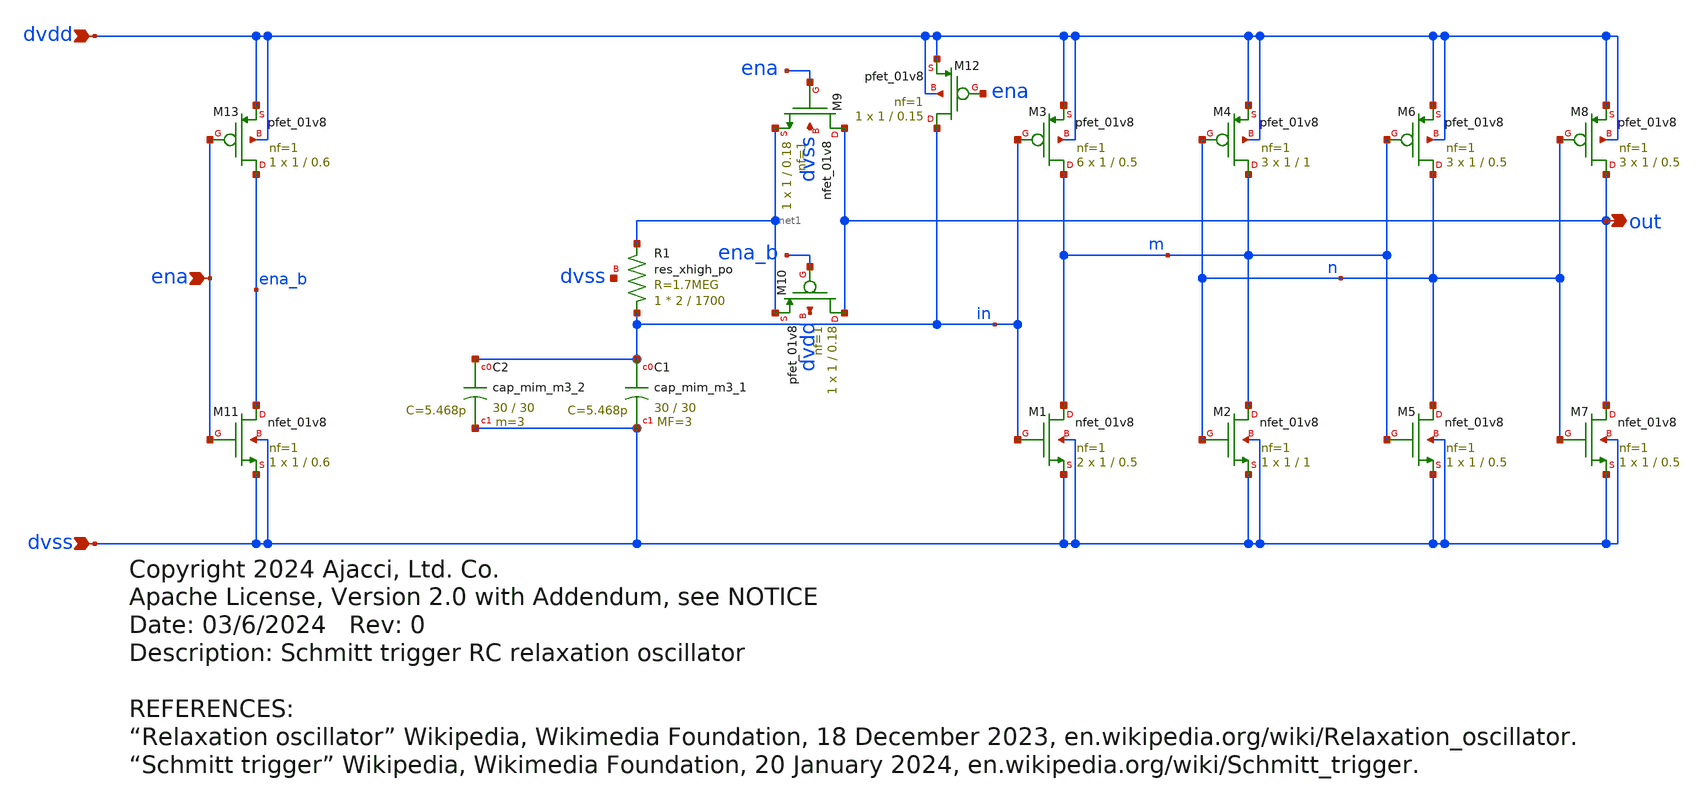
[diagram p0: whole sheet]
** sch_path: xschem/rc_osc.sch
* Copyright 2024 Ajacci, Ltd. Co.
* Apache License, Version 2.0 with Addendum, see NOTICE
**.subckt rc_osc dvdd dvss out ena
*.ipin dvdd
*.ipin dvss
*.opin out
*.ipin ena
XM1 m in dvss dvss sky130_fd_pr__nfet_01v8 L=0.5 W=1 nf=1 ad='int((nf+1)/2) * W/nf * 0.29' as='int((nf+2)/2) * W/nf * 0.29'
+ pd='2*int((nf+1)/2) * (W/nf + 0.29)' ps='2*int((nf+2)/2) * (W/nf + 0.29)' nrd='0.29 / W' nrs='0.29 / W'
+ sa=0 sb=0 sd=0 mult=2 m=2
XM3 m in dvdd dvdd sky130_fd_pr__pfet_01v8 L=0.5 W=1 nf=1 ad='int((nf+1)/2) * W/nf * 0.29' as='int((nf+2)/2) * W/nf * 0.29'
+ pd='2*int((nf+1)/2) * (W/nf + 0.29)' ps='2*int((nf+2)/2) * (W/nf + 0.29)' nrd='0.29 / W' nrs='0.29 / W'
+ sa=0 sb=0 sd=0 mult=6 m=6
XM2 m n dvss dvss sky130_fd_pr__nfet_01v8 L=1 W=1 nf=1 ad='int((nf+1)/2) * W/nf * 0.29' as='int((nf+2)/2) * W/nf * 0.29'
+ pd='2*int((nf+1)/2) * (W/nf + 0.29)' ps='2*int((nf+2)/2) * (W/nf + 0.29)' nrd='0.29 / W' nrs='0.29 / W'
+ sa=0 sb=0 sd=0 mult=1 m=1
XM4 m n dvdd dvdd sky130_fd_pr__pfet_01v8 L=1 W=1 nf=1 ad='int((nf+1)/2) * W/nf * 0.29' as='int((nf+2)/2) * W/nf * 0.29'
+ pd='2*int((nf+1)/2) * (W/nf + 0.29)' ps='2*int((nf+2)/2) * (W/nf + 0.29)' nrd='0.29 / W' nrs='0.29 / W'
+ sa=0 sb=0 sd=0 mult=3 m=3
XM5 n m dvss dvss sky130_fd_pr__nfet_01v8 L=0.5 W=1 nf=1 ad='int((nf+1)/2) * W/nf * 0.29' as='int((nf+2)/2) * W/nf * 0.29'
+ pd='2*int((nf+1)/2) * (W/nf + 0.29)' ps='2*int((nf+2)/2) * (W/nf + 0.29)' nrd='0.29 / W' nrs='0.29 / W'
+ sa=0 sb=0 sd=0 mult=1 m=1
XM6 n m dvdd dvdd sky130_fd_pr__pfet_01v8 L=0.5 W=1 nf=1 ad='int((nf+1)/2) * W/nf * 0.29' as='int((nf+2)/2) * W/nf * 0.29'
+ pd='2*int((nf+1)/2) * (W/nf + 0.29)' ps='2*int((nf+2)/2) * (W/nf + 0.29)' nrd='0.29 / W' nrs='0.29 / W'
+ sa=0 sb=0 sd=0 mult=3 m=3
XM7 out n dvss dvss sky130_fd_pr__nfet_01v8 L=0.5 W=1 nf=1 ad='int((nf+1)/2) * W/nf * 0.29' as='int((nf+2)/2) * W/nf * 0.29'
+ pd='2*int((nf+1)/2) * (W/nf + 0.29)' ps='2*int((nf+2)/2) * (W/nf + 0.29)' nrd='0.29 / W' nrs='0.29 / W'
+ sa=0 sb=0 sd=0 mult=1 m=1
XM8 out n dvdd dvdd sky130_fd_pr__pfet_01v8 L=0.5 W=1 nf=1 ad='int((nf+1)/2) * W/nf * 0.29' as='int((nf+2)/2) * W/nf * 0.29'
+ pd='2*int((nf+1)/2) * (W/nf + 0.29)' ps='2*int((nf+2)/2) * (W/nf + 0.29)' nrd='0.29 / W' nrs='0.29 / W'
+ sa=0 sb=0 sd=0 mult=3 m=3
XC1 in dvss sky130_fd_pr__cap_mim_m3_1 W=30 L=30 MF=3 m=3
XR1 in net1 dvss sky130_fd_pr__res_xhigh_po W=2 L=1700 mult=1 m=1
XM12 in ena dvdd dvdd sky130_fd_pr__pfet_01v8 L=0.15 W=1 nf=1 ad='int((nf+1)/2) * W/nf * 0.29' as='int((nf+2)/2) * W/nf * 0.29'
+ pd='2*int((nf+1)/2) * (W/nf + 0.29)' ps='2*int((nf+2)/2) * (W/nf + 0.29)' nrd='0.29 / W' nrs='0.29 / W'
+ sa=0 sb=0 sd=0 mult=1 m=1
XC2 in dvss sky130_fd_pr__cap_mim_m3_2 W=30 L=30 MF=3 m=3
XM9 out ena net1 dvss sky130_fd_pr__nfet_01v8 L=0.18 W=1 nf=1 ad='int((nf+1)/2) * W/nf * 0.29' as='int((nf+2)/2) * W/nf * 0.29'
+ pd='2*int((nf+1)/2) * (W/nf + 0.29)' ps='2*int((nf+2)/2) * (W/nf + 0.29)' nrd='0.29 / W' nrs='0.29 / W'
+ sa=0 sb=0 sd=0 mult=1 m=1
XM10 out ena_b net1 dvdd sky130_fd_pr__pfet_01v8 L=0.18 W=1 nf=1 ad='int((nf+1)/2) * W/nf * 0.29' as='int((nf+2)/2) * W/nf * 0.29'
+ pd='2*int((nf+1)/2) * (W/nf + 0.29)' ps='2*int((nf+2)/2) * (W/nf + 0.29)' nrd='0.29 / W' nrs='0.29 / W'
+ sa=0 sb=0 sd=0 mult=1 m=1
XM11 ena_b ena dvss dvss sky130_fd_pr__nfet_01v8 L=0.6 W=1 nf=1 ad='int((nf+1)/2) * W/nf * 0.29' as='int((nf+2)/2) * W/nf * 0.29'
+ pd='2*int((nf+1)/2) * (W/nf + 0.29)' ps='2*int((nf+2)/2) * (W/nf + 0.29)' nrd='0.29 / W' nrs='0.29 / W'
+ sa=0 sb=0 sd=0 mult=1 m=1
XM13 ena_b ena dvdd dvdd sky130_fd_pr__pfet_01v8 L=0.6 W=1 nf=1 ad='int((nf+1)/2) * W/nf * 0.29' as='int((nf+2)/2) * W/nf * 0.29'
+ pd='2*int((nf+1)/2) * (W/nf + 0.29)' ps='2*int((nf+2)/2) * (W/nf + 0.29)' nrd='0.29 / W' nrs='0.29 / W'
+ sa=0 sb=0 sd=0 mult=1 m=1
**.ends
.end
